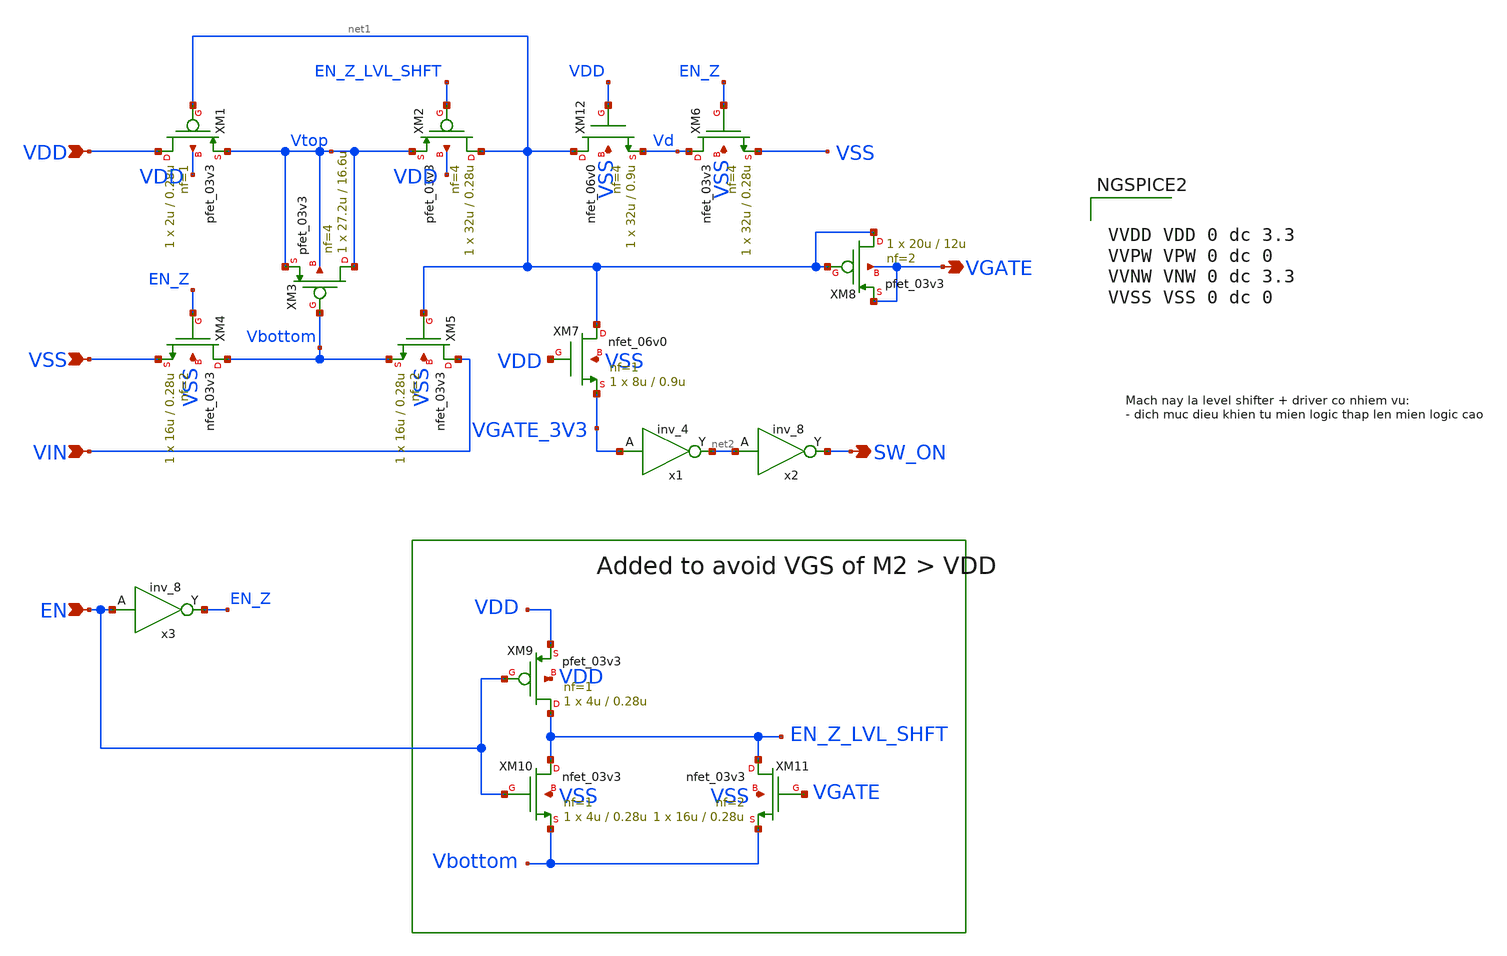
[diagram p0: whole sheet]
** sch_path: Schematic/bootstrap/bootstrap.sch
**.subckt bootstrap VDD VSS VIN VGATE EN SW_ON
*.ipin VDD
*.ipin VSS
*.ipin VIN
*.opin VGATE
*.ipin EN
*.opin SW_ON
XM1 VDD net1 Vtop VDD pfet_03v3 L=0.28u W=2u nf=1 ad='int((nf+1)/2) * W/nf * 0.18u' as='int((nf+2)/2) * W/nf * 0.18u'
+ pd='2*int((nf+1)/2) * (W/nf + 0.18u)' ps='2*int((nf+2)/2) * (W/nf + 0.18u)' nrd='0.18u / W' nrs='0.18u / W'
+ sa=0 sb=0 sd=0 m=1
XM2 net1 EN_Z_LVL_SHFT Vtop VDD pfet_03v3 L=0.28u W=32u nf=4 ad='int((nf+1)/2) * W/nf * 0.18u' as='int((nf+2)/2) * W/nf * 0.18u'
+ pd='2*int((nf+1)/2) * (W/nf + 0.18u)' ps='2*int((nf+2)/2) * (W/nf + 0.18u)' nrd='0.18u / W' nrs='0.18u / W'
+ sa=0 sb=0 sd=0 m=1
XM3 Vtop Vbottom Vtop Vtop pfet_03v3 L=16.6u W=27.2u nf=4 ad='int((nf+1)/2) * W/nf * 0.18u' as='int((nf+2)/2) * W/nf * 0.18u'
+ pd='2*int((nf+1)/2) * (W/nf + 0.18u)' ps='2*int((nf+2)/2) * (W/nf + 0.18u)' nrd='0.18u / W' nrs='0.18u / W'
+ sa=0 sb=0 sd=0 m=1
XM4 Vbottom EN_Z VSS VSS nfet_03v3 L=0.28u W=16u nf=2 ad='int((nf+1)/2) * W/nf * 0.18u' as='int((nf+2)/2) * W/nf * 0.18u'
+ pd='2*int((nf+1)/2) * (W/nf + 0.18u)' ps='2*int((nf+2)/2) * (W/nf + 0.18u)' nrd='0.18u / W' nrs='0.18u / W'
+ sa=0 sb=0 sd=0 m=1
XM5 VIN net1 Vbottom VSS nfet_03v3 L=0.28u W=16u nf=2 ad='int((nf+1)/2) * W/nf * 0.18u' as='int((nf+2)/2) * W/nf * 0.18u'
+ pd='2*int((nf+1)/2) * (W/nf + 0.18u)' ps='2*int((nf+2)/2) * (W/nf + 0.18u)' nrd='0.18u / W' nrs='0.18u / W'
+ sa=0 sb=0 sd=0 m=1
XM6 Vd EN_Z VSS VSS nfet_03v3 L=0.28u W=32u nf=4 ad='int((nf+1)/2) * W/nf * 0.18u' as='int((nf+2)/2) * W/nf * 0.18u'
+ pd='2*int((nf+1)/2) * (W/nf + 0.18u)' ps='2*int((nf+2)/2) * (W/nf + 0.18u)' nrd='0.18u / W' nrs='0.18u / W'
+ sa=0 sb=0 sd=0 m=1
XM9 EN_Z_LVL_SHFT EN VDD VDD pfet_03v3 L=0.28u W=4u nf=1 ad='int((nf+1)/2) * W/nf * 0.18u' as='int((nf+2)/2) * W/nf * 0.18u'
+ pd='2*int((nf+1)/2) * (W/nf + 0.18u)' ps='2*int((nf+2)/2) * (W/nf + 0.18u)' nrd='0.18u / W' nrs='0.18u / W'
+ sa=0 sb=0 sd=0 m=1
XM10 EN_Z_LVL_SHFT EN Vbottom VSS nfet_03v3 L=0.28u W=4u nf=1 ad='int((nf+1)/2) * W/nf * 0.18u' as='int((nf+2)/2) * W/nf * 0.18u'
+ pd='2*int((nf+1)/2) * (W/nf + 0.18u)' ps='2*int((nf+2)/2) * (W/nf + 0.18u)' nrd='0.18u / W' nrs='0.18u / W'
+ sa=0 sb=0 sd=0 m=1
XM11 EN_Z_LVL_SHFT VGATE Vbottom VSS nfet_03v3 L=0.28u W=16u nf=2 ad='int((nf+1)/2) * W/nf * 0.18u' as='int((nf+2)/2) * W/nf * 0.18u'
+ pd='2*int((nf+1)/2) * (W/nf + 0.18u)' ps='2*int((nf+2)/2) * (W/nf + 0.18u)' nrd='0.18u / W' nrs='0.18u / W'
+ sa=0 sb=0 sd=0 m=1
x1 VGATE_3V3 VGND VNB VPB VPWR net2 gf180mcu_fd_sc_mcu7t5v0__inv_4
XM12 net1 VDD Vd VSS nfet_06v0 L=0.9u W=32u nf=4 ad='int((nf+1)/2) * W/nf * 0.18u' as='int((nf+2)/2) * W/nf * 0.18u'
+ pd='2*int((nf+1)/2) * (W/nf + 0.18u)' ps='2*int((nf+2)/2) * (W/nf + 0.18u)' nrd='0.18u / W' nrs='0.18u / W'
+ sa=0 sb=0 sd=0 m=1
XM7 net1 VDD VGATE_3V3 VSS nfet_06v0 L=0.9u W=8u nf=1 ad='int((nf+1)/2) * W/nf * 0.18u' as='int((nf+2)/2) * W/nf * 0.18u'
+ pd='2*int((nf+1)/2) * (W/nf + 0.18u)' ps='2*int((nf+2)/2) * (W/nf + 0.18u)' nrd='0.18u / W' nrs='0.18u / W'
+ sa=0 sb=0 sd=0 m=1
x2 net2 VGND VNB VPB VPWR SW_ON gf180mcu_fd_sc_mcu7t5v0__inv_8
x3 EN VGND VNB VPB VPWR EN_Z gf180mcu_fd_sc_mcu7t5v0__inv_8
XM8 net1 net1 VGATE VGATE pfet_03v3 L=12u W=20u nf=2 ad='int((nf+1)/2) * W/nf * 0.18u' as='int((nf+2)/2) * W/nf * 0.18u'
+ pd='2*int((nf+1)/2) * (W/nf + 0.18u)' ps='2*int((nf+2)/2) * (W/nf + 0.18u)' nrd='0.18u / W' nrs='0.18u / W'
+ sa=0 sb=0 sd=0 m=1
**** begin user architecture code


VVDD VDD 0 dc 3.3
VVPW VPW 0 dc 0
VVNW VNW 0 dc 3.3
VVSS VSS 0 dc 0


**** end user architecture code
**.ends
.end
